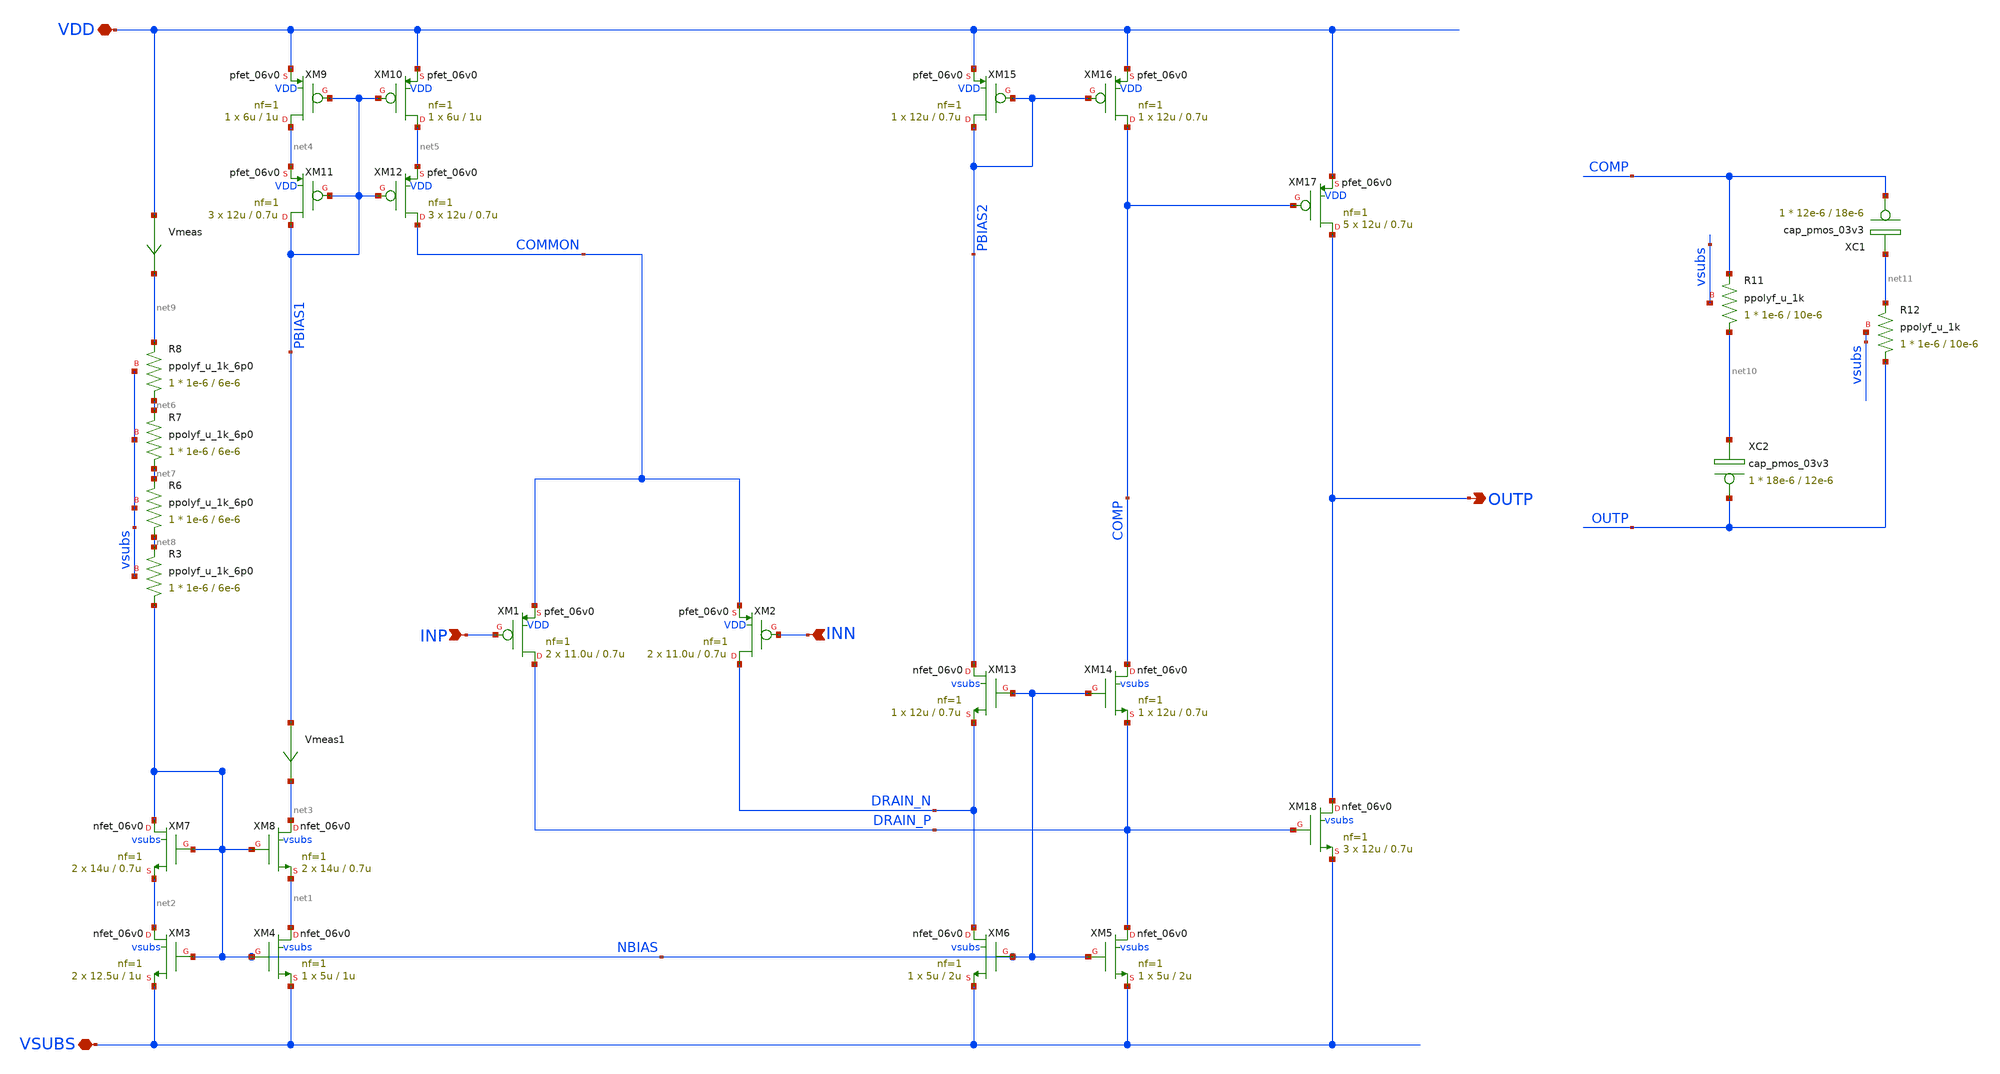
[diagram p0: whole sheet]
** sch_path: xschem/ip_amplifier.sch
**.subckt ip_amplifier VDD VSUBS INP INN OUTP
*.iopin VDD
*.iopin VSUBS
*.ipin INP
*.ipin INN
*.opin OUTP
XM1 DRAIN_P INP COMMON VDD pfet_06v0 L=0.7u W=11.0u nf=1 ad='int((nf+1)/2) * W/nf * 0.18u' as='int((nf+2)/2) * W/nf * 0.18u'
+ pd='2*int((nf+1)/2) * (W/nf + 0.18u)' ps='2*int((nf+2)/2) * (W/nf + 0.18u)' nrd='0.18u / W' nrs='0.18u / W'
+ sa=0 sb=0 sd=0 m=2 par=2
XM2 DRAIN_N INN COMMON VDD pfet_06v0 L=0.7u W=11.0u nf=1 ad='int((nf+1)/2) * W/nf * 0.18u' as='int((nf+2)/2) * W/nf * 0.18u'
+ pd='2*int((nf+1)/2) * (W/nf + 0.18u)' ps='2*int((nf+2)/2) * (W/nf + 0.18u)' nrd='0.18u / W' nrs='0.18u / W'
+ sa=0 sb=0 sd=0 m=2 par=2
XM5 DRAIN_P NBIAS VSUBS vsubs nfet_06v0 L=2u W=5u nf=1 ad='int((nf+1)/2) * W/nf * 0.18u' as='int((nf+2)/2) * W/nf * 0.18u'
+ pd='2*int((nf+1)/2) * (W/nf + 0.18u)' ps='2*int((nf+2)/2) * (W/nf + 0.18u)' nrd='0.18u / W' nrs='0.18u / W'
+ sa=0 sb=0 sd=0 m=1 par=1
XM6 DRAIN_N NBIAS VSUBS vsubs nfet_06v0 L=2u W=5u nf=1 ad='int((nf+1)/2) * W/nf * 0.18u' as='int((nf+2)/2) * W/nf * 0.18u'
+ pd='2*int((nf+1)/2) * (W/nf + 0.18u)' ps='2*int((nf+2)/2) * (W/nf + 0.18u)' nrd='0.18u / W' nrs='0.18u / W'
+ sa=0 sb=0 sd=0 m=1 par=1
XM3 net2 NBIAS VSUBS vsubs nfet_06v0 L=1u W=12.5u nf=1 ad='int((nf+1)/2) * W/nf * 0.18u' as='int((nf+2)/2) * W/nf * 0.18u'
+ pd='2*int((nf+1)/2) * (W/nf + 0.18u)' ps='2*int((nf+2)/2) * (W/nf + 0.18u)' nrd='0.18u / W' nrs='0.18u / W'
+ sa=0 sb=0 sd=0 m=2 par=2
XM4 net1 NBIAS VSUBS vsubs nfet_06v0 L=1u W=5u nf=1 ad='int((nf+1)/2) * W/nf * 0.18u' as='int((nf+2)/2) * W/nf * 0.18u'
+ pd='2*int((nf+1)/2) * (W/nf + 0.18u)' ps='2*int((nf+2)/2) * (W/nf + 0.18u)' nrd='0.18u / W' nrs='0.18u / W'
+ sa=0 sb=0 sd=0 m=1 par=1
XM7 NBIAS NBIAS net2 vsubs nfet_06v0 L=0.7u W=14u nf=1 ad='int((nf+1)/2) * W/nf * 0.18u' as='int((nf+2)/2) * W/nf * 0.18u'
+ pd='2*int((nf+1)/2) * (W/nf + 0.18u)' ps='2*int((nf+2)/2) * (W/nf + 0.18u)' nrd='0.18u / W' nrs='0.18u / W'
+ sa=0 sb=0 sd=0 m=2 par=2
XM8 net3 NBIAS net1 vsubs nfet_06v0 L=0.7u W=14u nf=1 ad='int((nf+1)/2) * W/nf * 0.18u' as='int((nf+2)/2) * W/nf * 0.18u'
+ pd='2*int((nf+1)/2) * (W/nf + 0.18u)' ps='2*int((nf+2)/2) * (W/nf + 0.18u)' nrd='0.18u / W' nrs='0.18u / W'
+ sa=0 sb=0 sd=0 m=2 par=2
XM9 net4 PBIAS1 VDD VDD pfet_06v0 L=1u W=6u nf=1 ad='int((nf+1)/2) * W/nf * 0.18u' as='int((nf+2)/2) * W/nf * 0.18u'
+ pd='2*int((nf+1)/2) * (W/nf + 0.18u)' ps='2*int((nf+2)/2) * (W/nf + 0.18u)' nrd='0.18u / W' nrs='0.18u / W'
+ sa=0 sb=0 sd=0 m=1 par=1
XM10 net5 PBIAS1 VDD VDD pfet_06v0 L=1u W=6u nf=1 ad='int((nf+1)/2) * W/nf * 0.18u' as='int((nf+2)/2) * W/nf * 0.18u'
+ pd='2*int((nf+1)/2) * (W/nf + 0.18u)' ps='2*int((nf+2)/2) * (W/nf + 0.18u)' nrd='0.18u / W' nrs='0.18u / W'
+ sa=0 sb=0 sd=0 m=1 par=1
XM11 PBIAS1 PBIAS1 net4 VDD pfet_06v0 L=0.7u W=12u nf=1 ad='int((nf+1)/2) * W/nf * 0.18u' as='int((nf+2)/2) * W/nf * 0.18u'
+ pd='2*int((nf+1)/2) * (W/nf + 0.18u)' ps='2*int((nf+2)/2) * (W/nf + 0.18u)' nrd='0.18u / W' nrs='0.18u / W'
+ sa=0 sb=0 sd=0 m=3 par=3
XM12 COMMON PBIAS1 net5 VDD pfet_06v0 L=0.7u W=12u nf=1 ad='int((nf+1)/2) * W/nf * 0.18u' as='int((nf+2)/2) * W/nf * 0.18u'
+ pd='2*int((nf+1)/2) * (W/nf + 0.18u)' ps='2*int((nf+2)/2) * (W/nf + 0.18u)' nrd='0.18u / W' nrs='0.18u / W'
+ sa=0 sb=0 sd=0 m=3 par=3
XM13 PBIAS2 NBIAS DRAIN_N vsubs nfet_06v0 L=0.7u W=12u nf=1 ad='int((nf+1)/2) * W/nf * 0.18u' as='int((nf+2)/2) * W/nf * 0.18u'
+ pd='2*int((nf+1)/2) * (W/nf + 0.18u)' ps='2*int((nf+2)/2) * (W/nf + 0.18u)' nrd='0.18u / W' nrs='0.18u / W'
+ sa=0 sb=0 sd=0 m=1 par=1
XM14 COMP NBIAS DRAIN_P vsubs nfet_06v0 L=0.7u W=12u nf=1 ad='int((nf+1)/2) * W/nf * 0.18u' as='int((nf+2)/2) * W/nf * 0.18u'
+ pd='2*int((nf+1)/2) * (W/nf + 0.18u)' ps='2*int((nf+2)/2) * (W/nf + 0.18u)' nrd='0.18u / W' nrs='0.18u / W'
+ sa=0 sb=0 sd=0 m=1 par=1
XM15 PBIAS2 PBIAS2 VDD VDD pfet_06v0 L=0.7u W=12u nf=1 ad='int((nf+1)/2) * W/nf * 0.18u' as='int((nf+2)/2) * W/nf * 0.18u'
+ pd='2*int((nf+1)/2) * (W/nf + 0.18u)' ps='2*int((nf+2)/2) * (W/nf + 0.18u)' nrd='0.18u / W' nrs='0.18u / W'
+ sa=0 sb=0 sd=0 m=1 par=1
XM16 COMP PBIAS2 VDD VDD pfet_06v0 L=0.7u W=12u nf=1 ad='int((nf+1)/2) * W/nf * 0.18u' as='int((nf+2)/2) * W/nf * 0.18u'
+ pd='2*int((nf+1)/2) * (W/nf + 0.18u)' ps='2*int((nf+2)/2) * (W/nf + 0.18u)' nrd='0.18u / W' nrs='0.18u / W'
+ sa=0 sb=0 sd=0 m=1 par=1
XM17 OUTP COMP VDD VDD pfet_06v0 L=0.7u W=12u nf=1 ad='int((nf+1)/2) * W/nf * 0.18u' as='int((nf+2)/2) * W/nf * 0.18u'
+ pd='2*int((nf+1)/2) * (W/nf + 0.18u)' ps='2*int((nf+2)/2) * (W/nf + 0.18u)' nrd='0.18u / W' nrs='0.18u / W'
+ sa=0 sb=0 sd=0 m=5 par=5
XM18 OUTP DRAIN_P VSUBS vsubs nfet_06v0 L=0.7u W=12u nf=1 ad='int((nf+1)/2) * W/nf * 0.18u' as='int((nf+2)/2) * W/nf * 0.18u'
+ pd='2*int((nf+1)/2) * (W/nf + 0.18u)' ps='2*int((nf+2)/2) * (W/nf + 0.18u)' nrd='0.18u / W' nrs='0.18u / W'
+ sa=0 sb=0 sd=0 m=3 par=3
XR3 NBIAS net8 vsubs ppolyf_u_1k_6p0 r_width=1e-6 r_length=6e-6 m=1
XR6 net8 net7 vsubs ppolyf_u_1k_6p0 r_width=1e-6 r_length=6e-6 m=1
XR7 net7 net6 vsubs ppolyf_u_1k_6p0 r_width=1e-6 r_length=6e-6 m=1
XR8 net6 net9 vsubs ppolyf_u_1k_6p0 r_width=1e-6 r_length=6e-6 m=1
Vmeas VDD net9 0
Vmeas1 PBIAS1 net3 0
XR11 net10 COMP vsubs ppolyf_u_1k r_width=1e-6 r_length=10e-6 m=1
XR12 OUTP net11 vsubs ppolyf_u_1k r_width=1e-6 r_length=10e-6 m=1
XC1 COMP net11 cap_pmos_03v3 c_width=12e-6 c_length=18e-6 m=1
XC2 OUTP net10 cap_pmos_03v3 c_width=18e-6 c_length=12e-6 m=1
**.ends
.end
